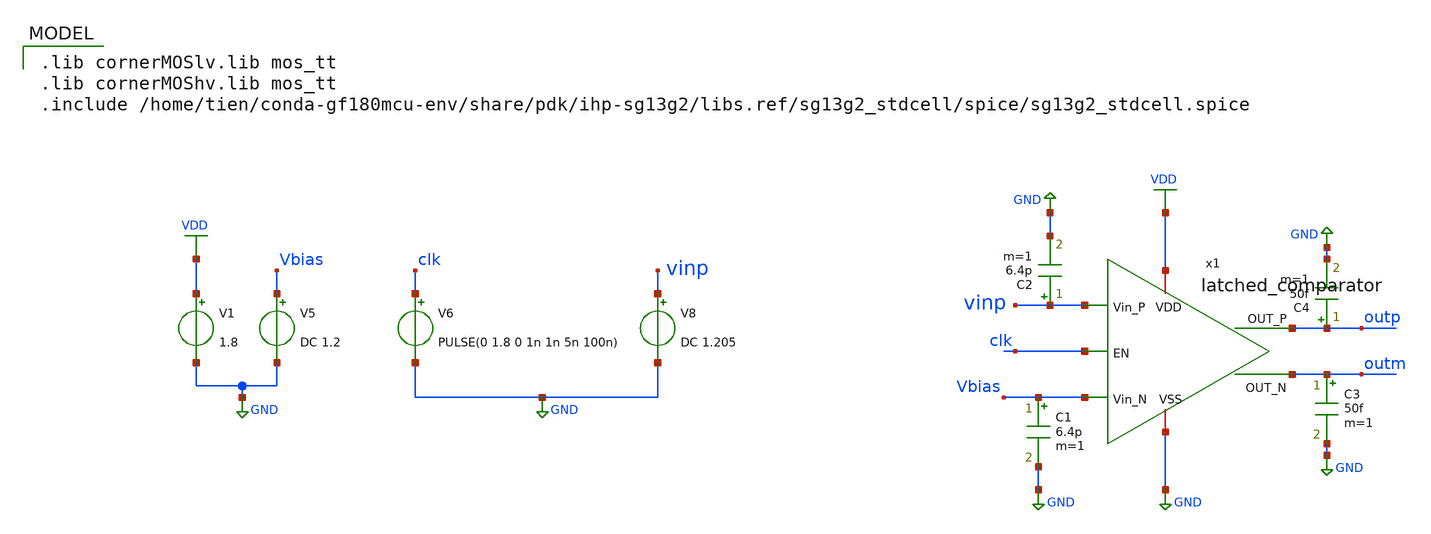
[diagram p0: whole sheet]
** sch_path: schematic/simulations/latch_comparator_tb2.sch
* IHP-GmbH/IHP-Open-PDK/ihp-sg13g2/libs.tech/xschem/sg13g2_stdcells/sg13g2_buf_4.sch:
* Copyright 2023 IHP PDK Authors
* Licensed under the Apache License, Version 2.0 (the "License");
**.subckt latch_comparator_tb2
x1 VDD vinp Vbias outp clk outm GND latched_comparator
V1 VDD GND 1.8
V5 Vbias GND DC 1.2
V6 clk GND PULSE(0 1.8 0 1n 1n 5n 100n)
V8 vinp GND DC 1.205
C1 Vbias GND 6.4p m=1
C4 outp GND 50f m=1
C2 vinp GND 6.4p m=1
C3 outm GND 50f m=1
**** begin user architecture code
 .lib cornerMOSlv.lib mos_tt
.lib cornerMOShv.lib mos_tt
.include /home/tien/conda-gf180mcu-env/share/pdk/ihp-sg13g2/libs.ref/sg13g2_stdcell/spice/sg13g2_stdcell.spice



.param temp=27
.param clock = 100e6       ; 100 MHz clock
.param period = {1/clock}
.param num_cycles = 100
.param tr = {num_cycles * period}

.control
save all
* Operating point simulation
op

set appendwrite

* Transient analysis
.options meas_step_max=1e-10
tran 500p 1u
let vindiff = v(vinp) - v(vbias)
let clk = v(clk)
let vout = v(outp) - v(outm)

meas TRAN rise_time TRIG v(outp) VAL=0.12  TD=9n RISE=4 TARG v(outp) VAL=1.08 TD=9n RISE=4
meas TRAN fall_time TRIG v(outp) VAL=1.08  TD=9n RISE=4 TARG v(outp) VAL=0.12 TD=9n RISE=4


.endc


**** end user architecture code
**.ends

* expanding   symbol:  latched_comparator/latched_comparator.sym # of pins=7
** sym_path: schematic/latched_comparator/latched_comparator.sym
** sch_path: schematic/latched_comparator/latched_comparator.sch
.subckt latched_comparator VDD Vin_P Vin_N OUT_P EN OUT_N VSS
*.ipin Vin_P
*.ipin Vin_N
*.iopin VDD
*.iopin VSS
*.ipin EN
*.opin OUT_P
*.opin OUT_N
XM1 net1 ENi VDD VDD sg13_lv_pmos w=0.32u l=0.15u ng=1 m=1 mm_ok=1
XM2 OUT_Ni ENi VDD VDD sg13_lv_pmos w=0.32u l=0.15u ng=1 m=1 mm_ok=1
XM3 OUT_Ni OUT_Pi VDD VDD sg13_lv_pmos w=1.25u l=0.15u ng=1 m=1 mm_ok=1
XM4 net2 ENi VDD VDD sg13_lv_pmos w=0.32u l=0.15u ng=1 m=1 mm_ok=1
XM5 OUT_Pi ENi VDD VDD sg13_lv_pmos w=0.32u l=0.15u ng=1 m=1 mm_ok=1
XM6 OUT_Pi OUT_Ni VDD VDD sg13_lv_pmos w=1.25u l=0.15u ng=1 m=1 mm_ok=1
XM7 net1 Vin_P net3 VSS sg13_lv_nmos w=0.55u l=0.13u ng=1 m=1 mm_ok=1
XM8 net2 Vin_N net3 VSS sg13_lv_nmos w=0.55u l=0.13u ng=1 m=1 mm_ok=1
XM9 OUT_Pi OUT_Ni net2 VSS sg13_lv_nmos w=0.42u l=0.15u ng=1 m=1 mm_ok=1
XM10 OUT_Ni OUT_Pi net1 VSS sg13_lv_nmos w=0.42u l=0.15u ng=1 m=1 mm_ok=1
XM11 net3 net3 net3 VSS sg13_lv_nmos w=0.55u l=0.13u ng=1 m=2 mm_ok=1
XM12 net3 ENi VSS VSS sg13_lv_nmos w=0.9u l=0.15u ng=1 m=2 mm_ok=1
x4 net4 OUT_Pi VDD VSS sg13g2_inv_2
x5 net5 OUT_Ni VDD VSS sg13g2_inv_2
x1 ENi EN VDD VSS sg13g2_buf_4
x6 OUT_P net4 VDD VSS sg13g2_inv_4
x2 OUT_N net5 VDD VSS sg13g2_inv_4
.ends


* expanding   symbol:  sg13g2_stdcells/sg13g2_inv_2.sym # of pins=2
** sym_path: sg13g2_stdcells/sg13g2_inv_2.sym
** sch_path: sg13g2_stdcells/sg13g2_inv_2.sch
.subckt sg13g2_inv_2 Y A VDD VSS
*.opin Y
*.ipin A
*.iopin VDD
*.iopin VSS
XM1 Y A VSS VSS sg13_lv_nmos w=1.48u l=130.00n ng=2 m=1 mm_ok=1
XM2 Y A VDD VDD sg13_lv_pmos w=2.24u l=130.00n ng=2 m=1 mm_ok=1
.ends


* expanding   symbol:  sg13g2_stdcells/sg13g2_buf_4.sym # of pins=2
** sym_path: sg13g2_stdcells/sg13g2_buf_4.sym
** sch_path: sg13g2_stdcells/sg13g2_buf_4.sch
.subckt sg13g2_buf_4 X A VDD VSS
*.ipin A
*.opin X
*.iopin VDD
*.iopin VSS
XM1 net1 A VSS VSS sg13_lv_nmos w=740.00n l=130.00n ng=1 m=1 mm_ok=1
XM2 X net1 VSS VSS sg13_lv_nmos w=2.96u l=130.00n ng=4 m=1 mm_ok=1
XM3 net1 A VDD VDD sg13_lv_pmos w=1.68u l=130.00n ng=2 m=1 mm_ok=1
XM4 X net1 VDD VDD sg13_lv_pmos w=4.48u l=130.00n ng=4 m=1 mm_ok=1
.ends


* expanding   symbol:  sg13g2_stdcells/sg13g2_inv_4.sym # of pins=2
** sym_path: sg13g2_stdcells/sg13g2_inv_4.sym
** sch_path: sg13g2_stdcells/sg13g2_inv_4.sch
.subckt sg13g2_inv_4 Y A VDD VSS
*.ipin A
*.opin Y
*.iopin VDD
*.iopin VSS
XM1 Y A VSS VSS sg13_lv_nmos w=2.96u l=130.00n ng=4 m=1 mm_ok=1
XM2 Y A VDD VDD sg13_lv_pmos w=4.48u l=130.00n ng=4 m=1 mm_ok=1
.ends

.GLOBAL VDD
.GLOBAL GND
.end
